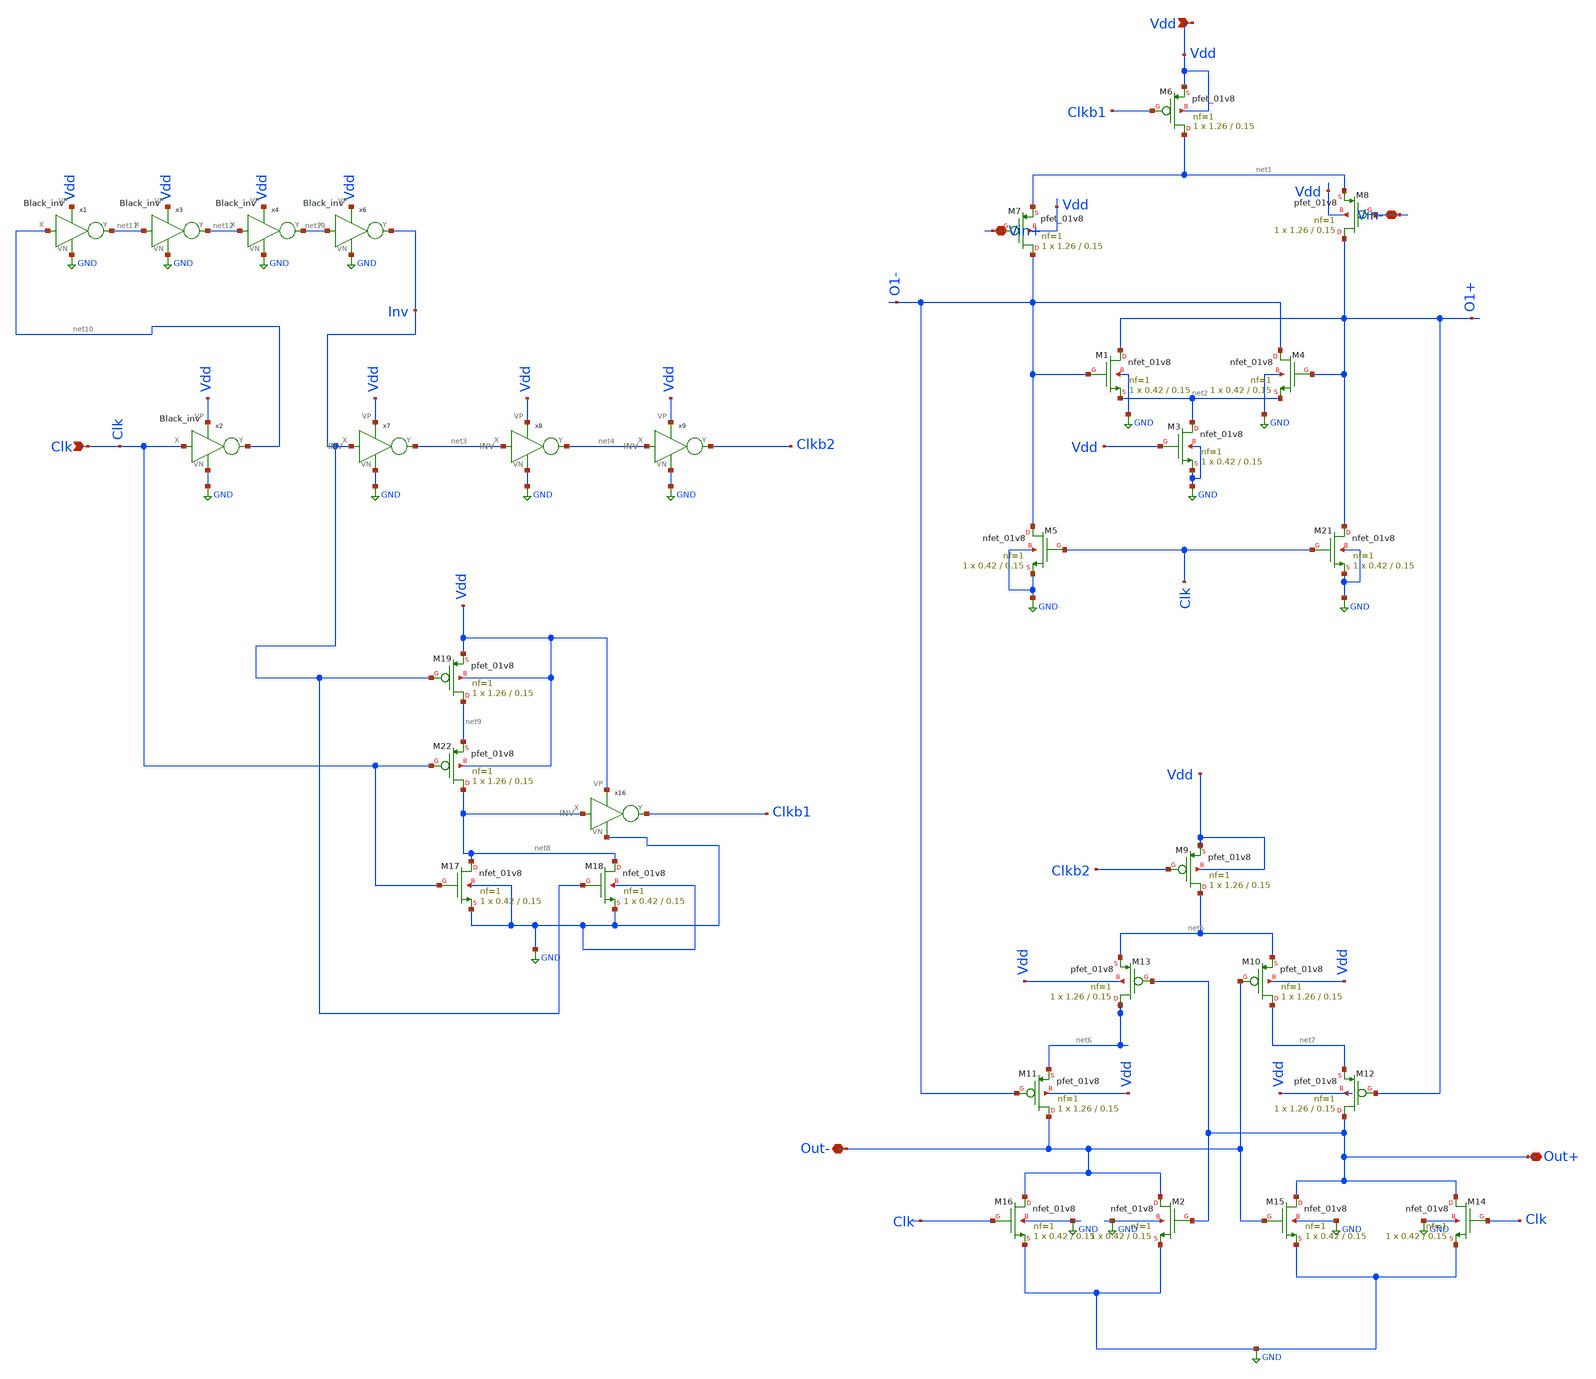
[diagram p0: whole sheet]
** sch_path: Blocks/comparator_150nm/Com_test_150_clkgen.sch
**.subckt Com_test_150_clkgen Vin+ Vin- Out+ Out- Vdd Clk
*.iopin Vin+
*.iopin Vin-
*.iopin Out+
*.iopin Out-
*.ipin Vdd
*.ipin Clk
XM6 net1 Clkb1 Vdd Vdd sky130_fd_pr__pfet_01v8 L=0.15 W=1.26 nf=1 ad='int((nf+1)/2) * W/nf * 0.29' as='int((nf+2)/2) * W/nf * 0.29'
+ pd='2*int((nf+1)/2) * (W/nf + 0.29)' ps='2*int((nf+2)/2) * (W/nf + 0.29)' nrd='0.29 / W' nrs='0.29 / W'
+ sa=0 sb=0 sd=0 mult=1 m=1
XM7 O1- Vin+ net1 Vdd sky130_fd_pr__pfet_01v8 L=0.15 W=1.26 nf=1 ad='int((nf+1)/2) * W/nf * 0.29' as='int((nf+2)/2) * W/nf * 0.29'
+ pd='2*int((nf+1)/2) * (W/nf + 0.29)' ps='2*int((nf+2)/2) * (W/nf + 0.29)' nrd='0.29 / W' nrs='0.29 / W'
+ sa=0 sb=0 sd=0 mult=1 m=1
XM8 O1+ Vin- net1 Vdd sky130_fd_pr__pfet_01v8 L=0.15 W=1.26 nf=1 ad='int((nf+1)/2) * W/nf * 0.29' as='int((nf+2)/2) * W/nf * 0.29'
+ pd='2*int((nf+1)/2) * (W/nf + 0.29)' ps='2*int((nf+2)/2) * (W/nf + 0.29)' nrd='0.29 / W' nrs='0.29 / W'
+ sa=0 sb=0 sd=0 mult=1 m=1
XM9 net5 Clkb2 Vdd Vdd sky130_fd_pr__pfet_01v8 L=0.15 W=1.26 nf=1 ad='int((nf+1)/2) * W/nf * 0.29' as='int((nf+2)/2) * W/nf * 0.29'
+ pd='2*int((nf+1)/2) * (W/nf + 0.29)' ps='2*int((nf+2)/2) * (W/nf + 0.29)' nrd='0.29 / W' nrs='0.29 / W'
+ sa=0 sb=0 sd=0 mult=1 m=1
XM10 net7 Out- net5 Vdd sky130_fd_pr__pfet_01v8 L=0.15 W=1.26 nf=1 ad='int((nf+1)/2) * W/nf * 0.29' as='int((nf+2)/2) * W/nf * 0.29'
+ pd='2*int((nf+1)/2) * (W/nf + 0.29)' ps='2*int((nf+2)/2) * (W/nf + 0.29)' nrd='0.29 / W' nrs='0.29 / W'
+ sa=0 sb=0 sd=0 mult=1 m=1
XM11 Out- O1- net6 Vdd sky130_fd_pr__pfet_01v8 L=0.15 W=1.26 nf=1 ad='int((nf+1)/2) * W/nf * 0.29' as='int((nf+2)/2) * W/nf * 0.29'
+ pd='2*int((nf+1)/2) * (W/nf + 0.29)' ps='2*int((nf+2)/2) * (W/nf + 0.29)' nrd='0.29 / W' nrs='0.29 / W'
+ sa=0 sb=0 sd=0 mult=1 m=1
XM12 Out+ O1+ net7 Vdd sky130_fd_pr__pfet_01v8 L=0.15 W=1.26 nf=1 ad='int((nf+1)/2) * W/nf * 0.29' as='int((nf+2)/2) * W/nf * 0.29'
+ pd='2*int((nf+1)/2) * (W/nf + 0.29)' ps='2*int((nf+2)/2) * (W/nf + 0.29)' nrd='0.29 / W' nrs='0.29 / W'
+ sa=0 sb=0 sd=0 mult=1 m=1
XM13 net6 Out+ net5 Vdd sky130_fd_pr__pfet_01v8 L=0.15 W=1.26 nf=1 ad='int((nf+1)/2) * W/nf * 0.29' as='int((nf+2)/2) * W/nf * 0.29'
+ pd='2*int((nf+1)/2) * (W/nf + 0.29)' ps='2*int((nf+2)/2) * (W/nf + 0.29)' nrd='0.29 / W' nrs='0.29 / W'
+ sa=0 sb=0 sd=0 mult=1 m=1
XM1 O1+ O1- net2 GND sky130_fd_pr__nfet_01v8 L=0.15 W=0.42 nf=1 ad='int((nf+1)/2) * W/nf * 0.29' as='int((nf+2)/2) * W/nf * 0.29'
+ pd='2*int((nf+1)/2) * (W/nf + 0.29)' ps='2*int((nf+2)/2) * (W/nf + 0.29)' nrd='0.29 / W' nrs='0.29 / W'
+ sa=0 sb=0 sd=0 mult=1 m=1
XM3 net2 Vdd GND GND sky130_fd_pr__nfet_01v8 L=0.15 W=0.42 nf=1 ad='int((nf+1)/2) * W/nf * 0.29' as='int((nf+2)/2) * W/nf * 0.29'
+ pd='2*int((nf+1)/2) * (W/nf + 0.29)' ps='2*int((nf+2)/2) * (W/nf + 0.29)' nrd='0.29 / W' nrs='0.29 / W'
+ sa=0 sb=0 sd=0 mult=1 m=1
XM4 O1- O1+ net2 GND sky130_fd_pr__nfet_01v8 L=0.15 W=0.42 nf=1 ad='int((nf+1)/2) * W/nf * 0.29' as='int((nf+2)/2) * W/nf * 0.29'
+ pd='2*int((nf+1)/2) * (W/nf + 0.29)' ps='2*int((nf+2)/2) * (W/nf + 0.29)' nrd='0.29 / W' nrs='0.29 / W'
+ sa=0 sb=0 sd=0 mult=1 m=1
XM5 O1- Clk GND GND sky130_fd_pr__nfet_01v8 L=0.15 W=0.42 nf=1 ad='int((nf+1)/2) * W/nf * 0.29' as='int((nf+2)/2) * W/nf * 0.29'
+ pd='2*int((nf+1)/2) * (W/nf + 0.29)' ps='2*int((nf+2)/2) * (W/nf + 0.29)' nrd='0.29 / W' nrs='0.29 / W'
+ sa=0 sb=0 sd=0 mult=1 m=1
XM21 O1+ Clk GND GND sky130_fd_pr__nfet_01v8 L=0.15 W=0.42 nf=1 ad='int((nf+1)/2) * W/nf * 0.29' as='int((nf+2)/2) * W/nf * 0.29'
+ pd='2*int((nf+1)/2) * (W/nf + 0.29)' ps='2*int((nf+2)/2) * (W/nf + 0.29)' nrd='0.29 / W' nrs='0.29 / W'
+ sa=0 sb=0 sd=0 mult=1 m=1
XM2 Out- Out+ GND GND sky130_fd_pr__nfet_01v8 L=0.15 W=0.42 nf=1 ad='int((nf+1)/2) * W/nf * 0.29' as='int((nf+2)/2) * W/nf * 0.29'
+ pd='2*int((nf+1)/2) * (W/nf + 0.29)' ps='2*int((nf+2)/2) * (W/nf + 0.29)' nrd='0.29 / W' nrs='0.29 / W'
+ sa=0 sb=0 sd=0 mult=1 m=1
XM14 Out+ Clk GND GND sky130_fd_pr__nfet_01v8 L=0.15 W=0.42 nf=1 ad='int((nf+1)/2) * W/nf * 0.29' as='int((nf+2)/2) * W/nf * 0.29'
+ pd='2*int((nf+1)/2) * (W/nf + 0.29)' ps='2*int((nf+2)/2) * (W/nf + 0.29)' nrd='0.29 / W' nrs='0.29 / W'
+ sa=0 sb=0 sd=0 mult=1 m=1
XM15 Out+ Out- GND GND sky130_fd_pr__nfet_01v8 L=0.15 W=0.42 nf=1 ad='int((nf+1)/2) * W/nf * 0.29' as='int((nf+2)/2) * W/nf * 0.29'
+ pd='2*int((nf+1)/2) * (W/nf + 0.29)' ps='2*int((nf+2)/2) * (W/nf + 0.29)' nrd='0.29 / W' nrs='0.29 / W'
+ sa=0 sb=0 sd=0 mult=1 m=1
XM16 Out- Clk GND GND sky130_fd_pr__nfet_01v8 L=0.15 W=0.42 nf=1 ad='int((nf+1)/2) * W/nf * 0.29' as='int((nf+2)/2) * W/nf * 0.29'
+ pd='2*int((nf+1)/2) * (W/nf + 0.29)' ps='2*int((nf+2)/2) * (W/nf + 0.29)' nrd='0.29 / W' nrs='0.29 / W'
+ sa=0 sb=0 sd=0 mult=1 m=1
XM17 net8 Clk GND GND sky130_fd_pr__nfet_01v8 L=0.15 W=0.42 nf=1 ad='int((nf+1)/2) * W/nf * 0.29' as='int((nf+2)/2) * W/nf * 0.29'
+ pd='2*int((nf+1)/2) * (W/nf + 0.29)' ps='2*int((nf+2)/2) * (W/nf + 0.29)' nrd='0.29 / W' nrs='0.29 / W'
+ sa=0 sb=0 sd=0 mult=1 m=1
XM18 net8 Inv GND GND sky130_fd_pr__nfet_01v8 L=0.15 W=0.42 nf=1 ad='int((nf+1)/2) * W/nf * 0.29' as='int((nf+2)/2) * W/nf * 0.29'
+ pd='2*int((nf+1)/2) * (W/nf + 0.29)' ps='2*int((nf+2)/2) * (W/nf + 0.29)' nrd='0.29 / W' nrs='0.29 / W'
+ sa=0 sb=0 sd=0 mult=1 m=1
XM19 net9 Inv Vdd Vdd sky130_fd_pr__pfet_01v8 L=0.15 W=1.26 nf=1 ad='int((nf+1)/2) * W/nf * 0.29' as='int((nf+2)/2) * W/nf * 0.29'
+ pd='2*int((nf+1)/2) * (W/nf + 0.29)' ps='2*int((nf+2)/2) * (W/nf + 0.29)' nrd='0.29 / W' nrs='0.29 / W'
+ sa=0 sb=0 sd=0 mult=1 m=1
XM22 net8 Clk net9 Vdd sky130_fd_pr__pfet_01v8 L=0.15 W=1.26 nf=1 ad='int((nf+1)/2) * W/nf * 0.29' as='int((nf+2)/2) * W/nf * 0.29'
+ pd='2*int((nf+1)/2) * (W/nf + 0.29)' ps='2*int((nf+2)/2) * (W/nf + 0.29)' nrd='0.29 / W' nrs='0.29 / W'
+ sa=0 sb=0 sd=0 mult=1 m=1
x1 net10 net11 Vdd GND black_inv
x2 Clk net10 Vdd GND black_inv
x3 net11 net12 Vdd GND black_inv
x4 net12 net13 Vdd GND black_inv
x6 net13 Inv Vdd GND black_inv
x7 Inv net3 Vdd GND INV
x8 net3 net4 Vdd GND INV
x9 net4 Clkb2 Vdd GND INV
x16 net8 Clkb1 Vdd GND INV
**.ends

* expanding   symbol:  component/black_inv_1/black_inv.sym # of pins=4
** sym_path: component/black_inv_1/black_inv.sym
** sch_path: component/black_inv_1/black_inv.sch
.subckt black_inv X Y VP VN
*.ipin X
*.opin Y
*.iopin VN
*.iopin VP
XM8 Y X VP VP sky130_fd_pr__pfet_01v8 L=.18 W=1.59 nf=1 ad='int((nf+1)/2) * W/nf * 0.29' as='int((nf+2)/2) * W/nf * 0.29'
+ pd='2*int((nf+1)/2) * (W/nf + 0.29)' ps='2*int((nf+2)/2) * (W/nf + 0.29)' nrd='0.29 / W' nrs='0.29 / W'
+ sa=0 sb=0 sd=0 mult=1 m=1
XM4 Y X VN VN sky130_fd_pr__nfet_01v8 L=0.18 W=0.502 nf=1 ad='int((nf+1)/2) * W/nf * 0.29' as='int((nf+2)/2) * W/nf * 0.29'
+ pd='2*int((nf+1)/2) * (W/nf + 0.29)' ps='2*int((nf+2)/2) * (W/nf + 0.29)' nrd='0.29 / W' nrs='0.29 / W'
+ sa=0 sb=0 sd=0 mult=1 m=1
.ends


* expanding   symbol:  component/Inverter/INV.sym # of pins=4
** sym_path: component/Inverter/INV.sym
** sch_path: component/Inverter/INV.sch
.subckt INV X Y VP VN
*.ipin X
*.opin Y
*.iopin VN
*.iopin VP
XM8 Y X VP VP sky130_fd_pr__pfet_01v8 L=.18 W=1.512 nf=1 ad='int((nf+1)/2) * W/nf * 0.29' as='int((nf+2)/2) * W/nf * 0.29'
+ pd='2*int((nf+1)/2) * (W/nf + 0.29)' ps='2*int((nf+2)/2) * (W/nf + 0.29)' nrd='0.29 / W' nrs='0.29 / W'
+ sa=0 sb=0 sd=0 mult=1 m=1
XM4 Y X VN VN sky130_fd_pr__nfet_01v8 L=0.18 W=0.42 nf=1 ad='int((nf+1)/2) * W/nf * 0.29' as='int((nf+2)/2) * W/nf * 0.29'
+ pd='2*int((nf+1)/2) * (W/nf + 0.29)' ps='2*int((nf+2)/2) * (W/nf + 0.29)' nrd='0.29 / W' nrs='0.29 / W'
+ sa=0 sb=0 sd=0 mult=1 m=1
.ends

.GLOBAL GND
.end
